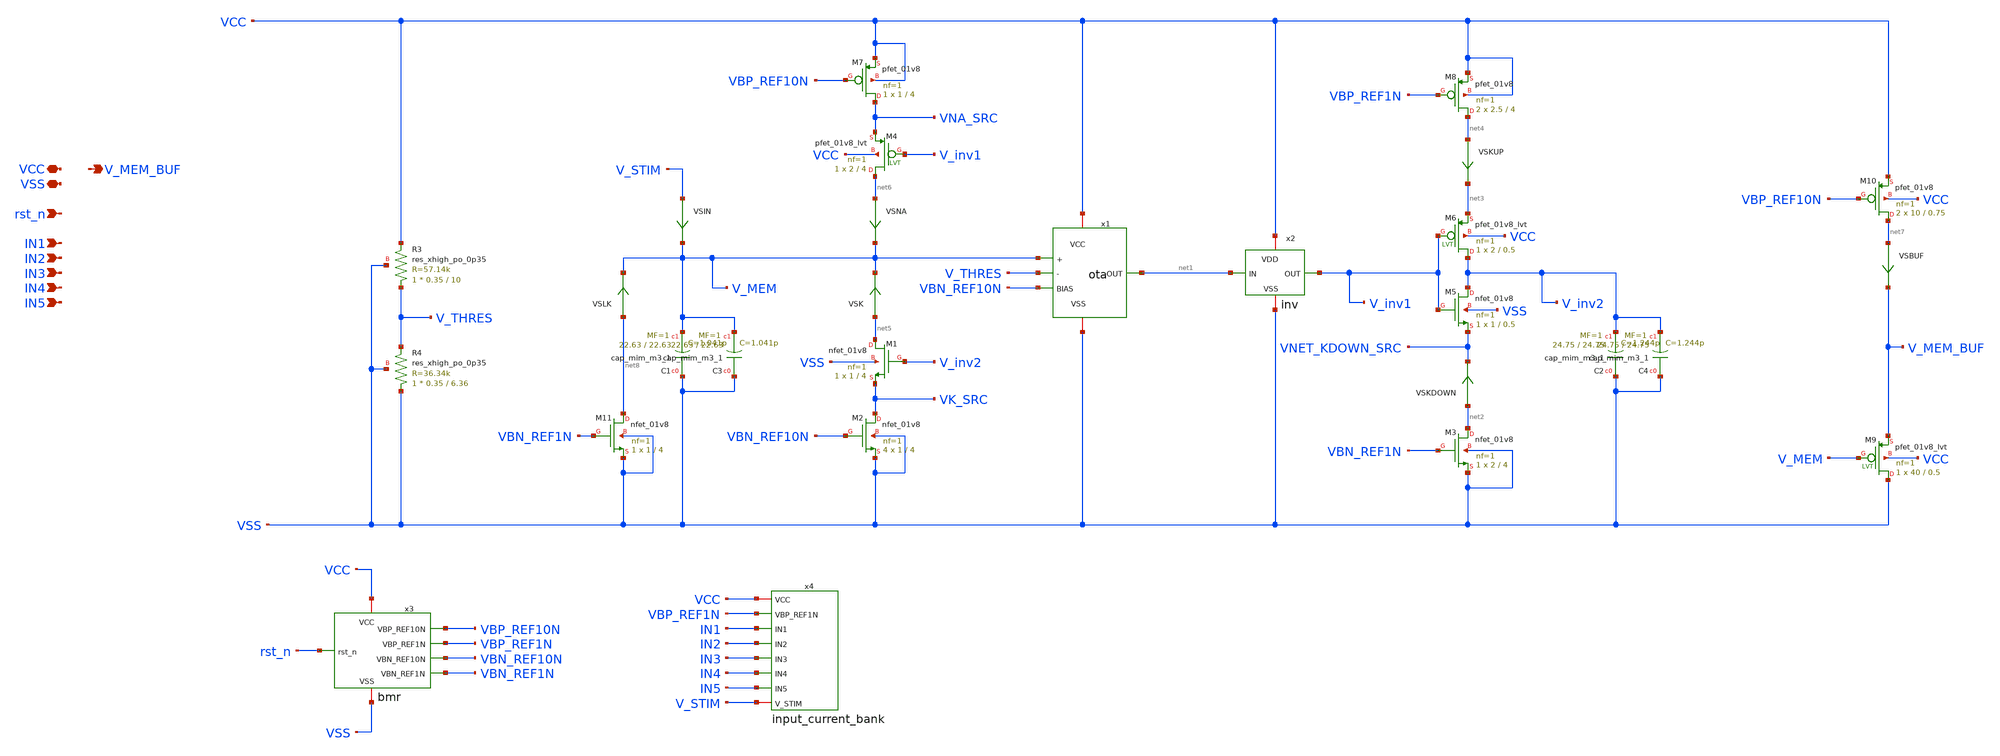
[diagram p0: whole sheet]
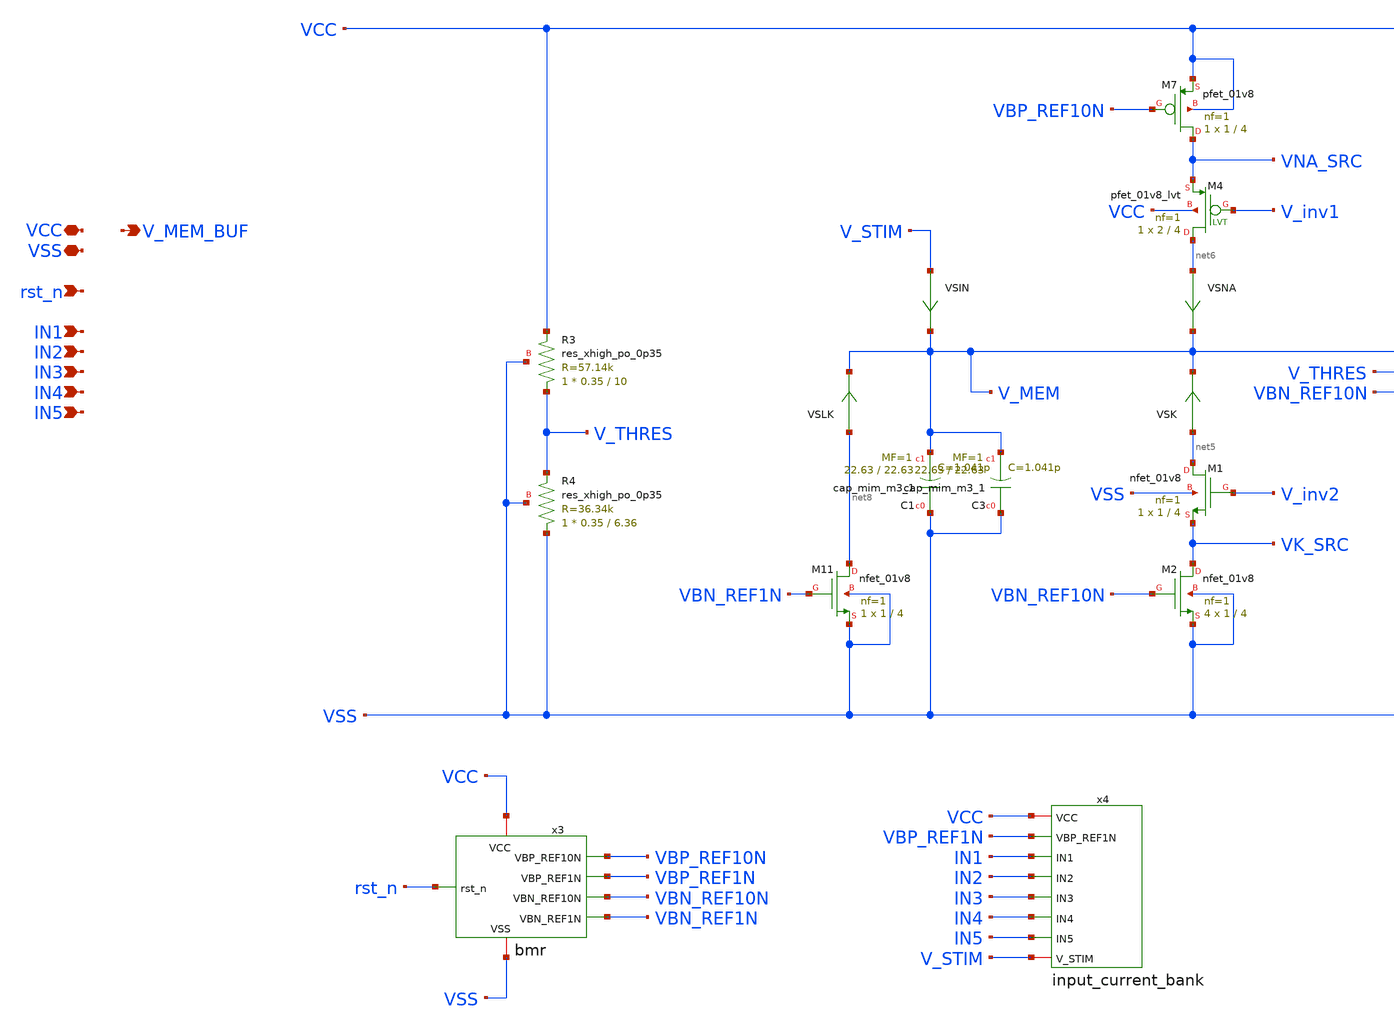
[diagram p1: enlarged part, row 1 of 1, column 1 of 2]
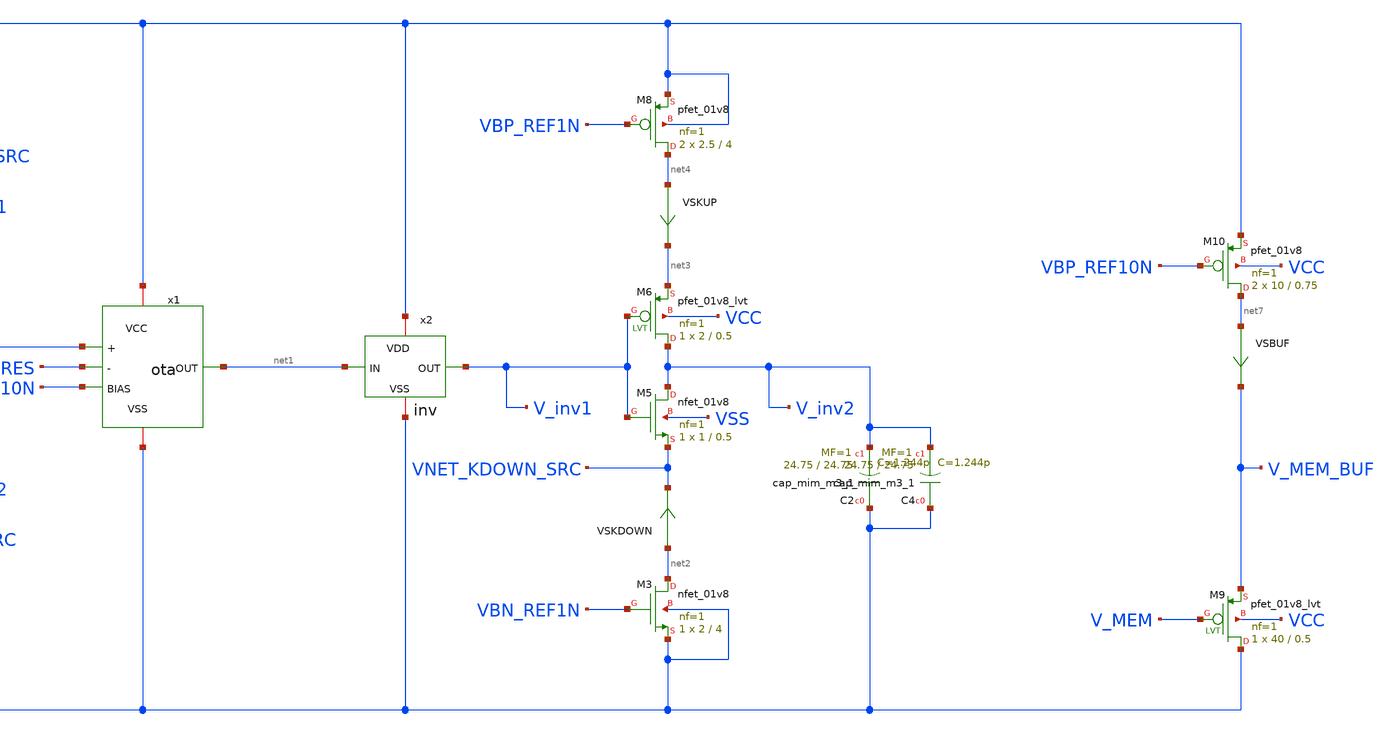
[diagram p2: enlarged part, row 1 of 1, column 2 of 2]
** sch_path: schem/vamp_if_neuron.sch
**.subckt vamp_if_neuron VCC VSS rst_n V_MEM_BUF IN1 IN2 IN3 IN4 IN5
*.iopin VCC
*.iopin VSS
*.ipin rst_n
*.opin V_MEM_BUF
*.ipin IN1
*.ipin IN2
*.ipin IN3
*.ipin IN4
*.ipin IN5
x1 VCC net1 VSS VBN_REF10N V_MEM V_THRES ota
x2 VCC net1 V_inv1 VSS inv
XC1 VSS V_MEM sky130_fd_pr__cap_mim_m3_1 W=22.63 L=22.63 MF=1 m=1
XM1 net5 V_inv2 VK_SRC VSS sky130_fd_pr__nfet_01v8 L=4 W=1 nf=1 ad='int((1 + 1)/2) * 1 / 1 * 0.29' as='int((1 + 2)/2) * 1 / 1 * 0.29'
+ pd='2*int((1 + 1)/2) * (1 / 1 + 0.29)' ps='2*int((1 + 2)/2) * (1 / 1 + 0.29)' nrd='0.29 / 1 ' nrs='0.29 / 1 '
+ sa=0 sb=0 sd=0 mult=1 m=1
XM5 V_inv2 V_inv1 VNET_KDOWN_SRC VSS sky130_fd_pr__nfet_01v8 L=0.5 W=1 nf=1 ad='int((1 + 1)/2) * 1 / 1 * 0.29'
+ as='int((1 + 2)/2) * 1 / 1 * 0.29' pd='2*int((1 + 1)/2) * (1 / 1 + 0.29)' ps='2*int((1 + 2)/2) * (1 / 1 + 0.29)'
+ nrd='0.29 / 1 ' nrs='0.29 / 1 ' sa=0 sb=0 sd=0 mult=1 m=1
XM6 V_inv2 V_inv1 net3 VCC sky130_fd_pr__pfet_01v8_lvt L=0.5 W=2 nf=1 ad='int((1 + 1)/2) * 2 / 1 * 0.29'
+ as='int((1 + 2)/2) * 2 / 1 * 0.29' pd='2*int((1 + 1)/2) * (2 / 1 + 0.29)' ps='2*int((1 + 2)/2) * (2 / 1 + 0.29)'
+ nrd='0.29 / 2 ' nrs='0.29 / 2 ' sa=0 sb=0 sd=0 mult=1 m=1
XC2 VSS V_inv2 sky130_fd_pr__cap_mim_m3_1 W=24.75 L=24.75 MF=1 m=1
VSNA net6 V_MEM 0
.save i(vsna)
VSKUP net4 net3 0
.save i(vskup)
VSK net5 V_MEM 0
.save i(vsk)
VSKDOWN net2 VNET_KDOWN_SRC 0
.save i(vskdown)
XM2 VK_SRC VBN_REF10N VSS VSS sky130_fd_pr__nfet_01v8 L=4 W=1 nf=1 ad='int((1 + 1)/2) * 1 / 1 * 0.29'
+ as='int((1 + 2)/2) * 1 / 1 * 0.29' pd='2*int((1 + 1)/2) * (1 / 1 + 0.29)' ps='2*int((1 + 2)/2) * (1 / 1 + 0.29)'
+ nrd='0.29 / 1 ' nrs='0.29 / 1 ' sa=0 sb=0 sd=0 mult=4 m=4
XM3 net2 VBN_REF1N VSS VSS sky130_fd_pr__nfet_01v8 L=4 W=2 nf=1 ad='int((1 + 1)/2) * 2 / 1 * 0.29' as='int((1 + 2)/2) * 2 / 1 * 0.29'
+ pd='2*int((1 + 1)/2) * (2 / 1 + 0.29)' ps='2*int((1 + 2)/2) * (2 / 1 + 0.29)' nrd='0.29 / 2 ' nrs='0.29 / 2 '
+ sa=0 sb=0 sd=0 mult=1 m=1
XM7 VNA_SRC VBP_REF10N VCC VCC sky130_fd_pr__pfet_01v8 L=4 W=1 nf=1 ad='int((1 + 1)/2) * 1 / 1 * 0.29'
+ as='int((1 + 2)/2) * 1 / 1 * 0.29' pd='2*int((1 + 1)/2) * (1 / 1 + 0.29)' ps='2*int((1 + 2)/2) * (1 / 1 + 0.29)'
+ nrd='0.29 / 1 ' nrs='0.29 / 1 ' sa=0 sb=0 sd=0 mult=1 m=1
XM8 net4 VBP_REF1N VCC VCC sky130_fd_pr__pfet_01v8 L=4 W=2.5 nf=1 ad='int((1 + 1)/2) * 2.5 / 1 * 0.29'
+ as='int((1 + 2)/2) * 2.5 / 1 * 0.29' pd='2*int((1 + 1)/2) * (2.5 / 1 + 0.29)' ps='2*int((1 + 2)/2) * (2.5 / 1 + 0.29)'
+ nrd='0.29 / 2.5 ' nrs='0.29 / 2.5 ' sa=0 sb=0 sd=0 mult=2 m=2
XM4 net6 V_inv1 VNA_SRC VCC sky130_fd_pr__pfet_01v8_lvt L=4 W=2 nf=1 ad='int((1 + 1)/2) * 2 / 1 * 0.29'
+ as='int((1 + 2)/2) * 2 / 1 * 0.29' pd='2*int((1 + 1)/2) * (2 / 1 + 0.29)' ps='2*int((1 + 2)/2) * (2 / 1 + 0.29)'
+ nrd='0.29 / 2 ' nrs='0.29 / 2 ' sa=0 sb=0 sd=0 mult=1 m=1
VSIN V_STIM V_MEM 0
.save i(vsin)
x3 VCC VBP_REF10N VSS VBP_REF1N VBN_REF10N VBN_REF1N rst_n bmr
VSBUF net7 V_MEM_BUF 0
.save i(vsbuf)
XM9 VSS V_MEM V_MEM_BUF VCC sky130_fd_pr__pfet_01v8_lvt L=0.5 W=40 nf=1 ad='int((1 + 1)/2) * 40 / 1 * 0.29'
+ as='int((1 + 2)/2) * 40 / 1 * 0.29' pd='2*int((1 + 1)/2) * (40 / 1 + 0.29)' ps='2*int((1 + 2)/2) * (40 / 1 + 0.29)'
+ nrd='0.29 / 40 ' nrs='0.29 / 40 ' sa=0 sb=0 sd=0 mult=1 m=1
XM10 net7 VBP_REF10N VCC VCC sky130_fd_pr__pfet_01v8 L=0.75 W=10 nf=1 ad='int((1 + 1)/2) * 10 / 1 * 0.29'
+ as='int((1 + 2)/2) * 10 / 1 * 0.29' pd='2*int((1 + 1)/2) * (10 / 1 + 0.29)' ps='2*int((1 + 2)/2) * (10 / 1 + 0.29)'
+ nrd='0.29 / 10 ' nrs='0.29 / 10 ' sa=0 sb=0 sd=0 mult=2 m=2
XM11 net8 VBN_REF1N VSS VSS sky130_fd_pr__nfet_01v8 L=4 W=1 nf=1 ad='int((1 + 1)/2) * 1 / 1 * 0.29' as='int((1 + 2)/2) * 1 / 1 * 0.29'
+ pd='2*int((1 + 1)/2) * (1 / 1 + 0.29)' ps='2*int((1 + 2)/2) * (1 / 1 + 0.29)' nrd='0.29 / 1 ' nrs='0.29 / 1 '
+ sa=0 sb=0 sd=0 mult=1 m=1
VSLK net8 V_MEM 0
.save i(vslk)
XR3 V_THRES VCC VSS sky130_fd_pr__res_xhigh_po_0p35 L=10 mult=1 m=1
XR4 VSS V_THRES VSS sky130_fd_pr__res_xhigh_po_0p35 L=6.36 mult=1 m=1
x4 VCC V_STIM VBP_REF1N IN1 IN2 IN3 IN4 IN5 input_current_bank
XC3 VSS V_MEM sky130_fd_pr__cap_mim_m3_1 W=22.63 L=22.63 MF=1 m=1
XC4 VSS V_inv2 sky130_fd_pr__cap_mim_m3_1 W=24.75 L=24.75 MF=1 m=1
**.ends

* expanding   symbol:  ota/ota.sym # of pins=6
** sym_path: schem/ota/ota.sym
** sch_path: schem/ota/ota.sch
.subckt ota VCC OUT VSS BIAS + -
*.ipin BIAS
*.ipin +
*.ipin -
*.opin OUT
*.iopin VCC
*.iopin VSS
XM1 VSRC + VBOT VSS sky130_fd_pr__nfet_01v8 L=0.5 W=1 nf=1 ad='int((1 + 1)/2) * 1 / 1 * 0.29' as='int((1 + 2)/2) * 1 / 1 * 0.29'
+ pd='2*int((1 + 1)/2) * (1 / 1 + 0.29)' ps='2*int((1 + 2)/2) * (1 / 1 + 0.29)' nrd='0.29 / 1 ' nrs='0.29 / 1 '
+ sa=0 sb=0 sd=0 mult=1 m=1
XM2 OUT - VBOT VSS sky130_fd_pr__nfet_01v8 L=0.5 W=1 nf=1 ad='int((1 + 1)/2) * 1 / 1 * 0.29' as='int((1 + 2)/2) * 1 / 1 * 0.29'
+ pd='2*int((1 + 1)/2) * (1 / 1 + 0.29)' ps='2*int((1 + 2)/2) * (1 / 1 + 0.29)' nrd='0.29 / 1 ' nrs='0.29 / 1 '
+ sa=0 sb=0 sd=0 mult=1 m=1
XM3 VSRC VSRC VCC VCC sky130_fd_pr__pfet_01v8_lvt L=0.5 W=2 nf=1 ad='int((1 + 1)/2) * 2 / 1 * 0.29' as='int((1 + 2)/2) * 2 / 1 * 0.29'
+ pd='2*int((1 + 1)/2) * (2 / 1 + 0.29)' ps='2*int((1 + 2)/2) * (2 / 1 + 0.29)' nrd='0.29 / 2 ' nrs='0.29 / 2 '
+ sa=0 sb=0 sd=0 mult=1 m=1
XM4 OUT VSRC VCC VCC sky130_fd_pr__pfet_01v8_lvt L=0.5 W=2 nf=1 ad='int((1 + 1)/2) * 2 / 1 * 0.29' as='int((1 + 2)/2) * 2 / 1 * 0.29'
+ pd='2*int((1 + 1)/2) * (2 / 1 + 0.29)' ps='2*int((1 + 2)/2) * (2 / 1 + 0.29)' nrd='0.29 / 2 ' nrs='0.29 / 2 '
+ sa=0 sb=0 sd=0 mult=1 m=1
XM5 VBOT BIAS VSS VSS sky130_fd_pr__nfet_01v8 L=0.5 W=1 nf=1 ad='int((1 + 1)/2) * 1 / 1 * 0.29' as='int((1 + 2)/2) * 1 / 1 * 0.29'
+ pd='2*int((1 + 1)/2) * (1 / 1 + 0.29)' ps='2*int((1 + 2)/2) * (1 / 1 + 0.29)' nrd='0.29 / 1 ' nrs='0.29 / 1 '
+ sa=0 sb=0 sd=0 mult=1 m=1
.ends


* expanding   symbol:  inv/inv.sym # of pins=4
** sym_path: schem/inv/inv.sym
** sch_path: schem/inv/inv.sch
.subckt inv VDD IN OUT VSS
*.ipin IN
*.iopin VDD
*.iopin VSS
*.opin OUT
XM1 OUT IN VSS VSS sky130_fd_pr__nfet_01v8 L=0.5 W=1 nf=1 ad='int((1 + 1)/2) * 1 / 1 * 0.29' as='int((1 + 2)/2) * 1 / 1 * 0.29'
+ pd='2*int((1 + 1)/2) * (1 / 1 + 0.29)' ps='2*int((1 + 2)/2) * (1 / 1 + 0.29)' nrd='0.29 / 1 ' nrs='0.29 / 1 '
+ sa=0 sb=0 sd=0 mult=1 m=1
XM2 OUT IN VDD VDD sky130_fd_pr__pfet_01v8_lvt L=0.5 W=2 nf=1 ad='int((1 + 1)/2) * 2 / 1 * 0.29' as='int((1 + 2)/2) * 2 / 1 * 0.29'
+ pd='2*int((1 + 1)/2) * (2 / 1 + 0.29)' ps='2*int((1 + 2)/2) * (2 / 1 + 0.29)' nrd='0.29 / 2 ' nrs='0.29 / 2 '
+ sa=0 sb=0 sd=0 mult=1 m=1
.ends


* expanding   symbol:  bias/bmr.sym # of pins=7
** sym_path: schem/bias/bmr.sym
** sch_path: schem/bias/bmr.sch
.subckt bmr VCC VBP_REF10N VSS VBP_REF1N VBN_REF10N VBN_REF1N rst_n
*.iopin VCC
*.iopin VSS
*.ipin rst_n
*.opin VBP_REF10N
*.opin VBP_REF1N
*.opin VBN_REF10N
*.opin VBN_REF1N
x1 VCC VBP_REF10N VSS VBN_REF10N rst_n bmr_10n
XM1 net1 VBP_REF10N VCC VCC sky130_fd_pr__pfet_01v8 L=4 W=1 nf=1 ad='int((1 + 1)/2) * 1 / 1 * 0.29' as='int((1 + 2)/2) * 1 / 1 * 0.29'
+ pd='2*int((1 + 1)/2) * (1 / 1 + 0.29)' ps='2*int((1 + 2)/2) * (1 / 1 + 0.29)' nrd='0.29 / 1 ' nrs='0.29 / 1 '
+ sa=0 sb=0 sd=0 mult=1 m=1
XM2 VBN_REF1N VBN_REF1N VSS VSS sky130_fd_pr__nfet_01v8 L=4 W=1 nf=1 ad='int((1 + 1)/2) * 1 / 1 * 0.29'
+ as='int((1 + 2)/2) * 1 / 1 * 0.29' pd='2*int((1 + 1)/2) * (1 / 1 + 0.29)' ps='2*int((1 + 2)/2) * (1 / 1 + 0.29)'
+ nrd='0.29 / 1 ' nrs='0.29 / 1 ' sa=0 sb=0 sd=0 mult=10 m=10
XM3 net2 VBN_REF1N VSS VSS sky130_fd_pr__nfet_01v8 L=4 W=1 nf=1 ad='int((1 + 1)/2) * 1 / 1 * 0.29' as='int((1 + 2)/2) * 1 / 1 * 0.29'
+ pd='2*int((1 + 1)/2) * (1 / 1 + 0.29)' ps='2*int((1 + 2)/2) * (1 / 1 + 0.29)' nrd='0.29 / 1 ' nrs='0.29 / 1 '
+ sa=0 sb=0 sd=0 mult=1 m=1
XM4 VBP_REF1N VBP_REF1N VCC VCC sky130_fd_pr__pfet_01v8 L=4 W=1 nf=1 ad='int((1 + 1)/2) * 1 / 1 * 0.29'
+ as='int((1 + 2)/2) * 1 / 1 * 0.29' pd='2*int((1 + 1)/2) * (1 / 1 + 0.29)' ps='2*int((1 + 2)/2) * (1 / 1 + 0.29)'
+ nrd='0.29 / 1 ' nrs='0.29 / 1 ' sa=0 sb=0 sd=0 mult=1 m=1
Vmeas net1 VBN_REF1N 0
.save i(vmeas)
Vmeas1 VBP_REF1N net2 0
.save i(vmeas1)
.ends


* expanding   symbol:  input_current_bank.sym # of pins=8
** sym_path: schem/input_current_bank.sym
** sch_path: schem/input_current_bank.sch
.subckt input_current_bank VCC V_STIM VBP_REF1N IN1 IN2 IN3 IN4 IN5
*.iopin VCC
*.iopin V_STIM
*.ipin VBP_REF1N
*.ipin IN1
*.ipin IN2
*.ipin IN3
*.ipin IN4
*.ipin IN5
X0.5 net1 VBP_REF1N VCC VCC sky130_fd_pr__pfet_01v8 L=16 W=0.5 nf=1 ad='int((1 + 1)/2) * 0.5 / 1 * 0.29'
+ as='int((1 + 2)/2) * 0.5 / 1 * 0.29' pd='2*int((1 + 1)/2) * (0.5 / 1 + 0.29)' ps='2*int((1 + 2)/2) * (0.5 / 1 + 0.29)'
+ nrd='0.29 / 0.5 ' nrs='0.29 / 0.5 ' sa=0 sb=0 sd=0 mult=1 m=1
XM13 V_STIM IN1 net1 VCC sky130_fd_pr__pfet_01v8_lvt L=4 W=2 nf=1 ad='int((1 + 1)/2) * 2 / 1 * 0.29'
+ as='int((1 + 2)/2) * 2 / 1 * 0.29' pd='2*int((1 + 1)/2) * (2 / 1 + 0.29)' ps='2*int((1 + 2)/2) * (2 / 1 + 0.29)'
+ nrd='0.29 / 2 ' nrs='0.29 / 2 ' sa=0 sb=0 sd=0 mult=1 m=1
XM14 net2 VBP_REF1N VCC VCC sky130_fd_pr__pfet_01v8 L=8 W=0.5 nf=1 ad='int((1 + 1)/2) * 0.5 / 1 * 0.29'
+ as='int((1 + 2)/2) * 0.5 / 1 * 0.29' pd='2*int((1 + 1)/2) * (0.5 / 1 + 0.29)' ps='2*int((1 + 2)/2) * (0.5 / 1 + 0.29)'
+ nrd='0.29 / 0.5 ' nrs='0.29 / 0.5 ' sa=0 sb=0 sd=0 mult=1 m=1
XM15 V_STIM IN2 net2 VCC sky130_fd_pr__pfet_01v8_lvt L=4 W=2 nf=1 ad='int((1 + 1)/2) * 2 / 1 * 0.29'
+ as='int((1 + 2)/2) * 2 / 1 * 0.29' pd='2*int((1 + 1)/2) * (2 / 1 + 0.29)' ps='2*int((1 + 2)/2) * (2 / 1 + 0.29)'
+ nrd='0.29 / 2 ' nrs='0.29 / 2 ' sa=0 sb=0 sd=0 mult=1 m=1
XM16 net3 VBP_REF1N VCC VCC sky130_fd_pr__pfet_01v8 L=4 W=1 nf=1 ad='int((1 + 1)/2) * 1 / 1 * 0.29' as='int((1 + 2)/2) * 1 / 1 * 0.29'
+ pd='2*int((1 + 1)/2) * (1 / 1 + 0.29)' ps='2*int((1 + 2)/2) * (1 / 1 + 0.29)' nrd='0.29 / 1 ' nrs='0.29 / 1 '
+ sa=0 sb=0 sd=0 mult=1 m=1
XM17 V_STIM IN3 net3 VCC sky130_fd_pr__pfet_01v8_lvt L=4 W=2 nf=1 ad='int((1 + 1)/2) * 2 / 1 * 0.29'
+ as='int((1 + 2)/2) * 2 / 1 * 0.29' pd='2*int((1 + 1)/2) * (2 / 1 + 0.29)' ps='2*int((1 + 2)/2) * (2 / 1 + 0.29)'
+ nrd='0.29 / 2 ' nrs='0.29 / 2 ' sa=0 sb=0 sd=0 mult=1 m=1
XM18 net4 VBP_REF1N VCC VCC sky130_fd_pr__pfet_01v8 L=4 W=1 nf=1 ad='int((1 + 1)/2) * 1 / 1 * 0.29' as='int((1 + 2)/2) * 1 / 1 * 0.29'
+ pd='2*int((1 + 1)/2) * (1 / 1 + 0.29)' ps='2*int((1 + 2)/2) * (1 / 1 + 0.29)' nrd='0.29 / 1 ' nrs='0.29 / 1 '
+ sa=0 sb=0 sd=0 mult=1 m=1
XM19 V_STIM IN4 net4 VCC sky130_fd_pr__pfet_01v8_lvt L=4 W=2 nf=1 ad='int((1 + 1)/2) * 2 / 1 * 0.29'
+ as='int((1 + 2)/2) * 2 / 1 * 0.29' pd='2*int((1 + 1)/2) * (2 / 1 + 0.29)' ps='2*int((1 + 2)/2) * (2 / 1 + 0.29)'
+ nrd='0.29 / 2 ' nrs='0.29 / 2 ' sa=0 sb=0 sd=0 mult=1 m=1
XM20 net5 VBP_REF1N VCC VCC sky130_fd_pr__pfet_01v8 L=4 W=1 nf=1 ad='int((1 + 1)/2) * 1 / 1 * 0.29' as='int((1 + 2)/2) * 1 / 1 * 0.29'
+ pd='2*int((1 + 1)/2) * (1 / 1 + 0.29)' ps='2*int((1 + 2)/2) * (1 / 1 + 0.29)' nrd='0.29 / 1 ' nrs='0.29 / 1 '
+ sa=0 sb=0 sd=0 mult=2 m=2
XM21 V_STIM IN5 net5 VCC sky130_fd_pr__pfet_01v8_lvt L=4 W=2 nf=1 ad='int((1 + 1)/2) * 2 / 1 * 0.29'
+ as='int((1 + 2)/2) * 2 / 1 * 0.29' pd='2*int((1 + 1)/2) * (2 / 1 + 0.29)' ps='2*int((1 + 2)/2) * (2 / 1 + 0.29)'
+ nrd='0.29 / 2 ' nrs='0.29 / 2 ' sa=0 sb=0 sd=0 mult=1 m=1
.ends


* expanding   symbol:  bias/bmr_10n.sym # of pins=5
** sym_path: schem/bias/bmr_10n.sym
** sch_path: schem/bias/bmr_10n.sch
.subckt bmr_10n VCC VBP VSS VBN rst_n
*.iopin VCC
*.iopin VSS
*.ipin rst_n
*.opin VBP
*.opin VBN
XM1 VBP VBP VCC VCC sky130_fd_pr__pfet_01v8 L=4 W=1 nf=1 ad='int((1 + 1)/2) * 1 / 1 * 0.29' as='int((1 + 2)/2) * 1 / 1 * 0.29'
+ pd='2*int((1 + 1)/2) * (1 / 1 + 0.29)' ps='2*int((1 + 2)/2) * (1 / 1 + 0.29)' nrd='0.29 / 1 ' nrs='0.29 / 1 '
+ sa=0 sb=0 sd=0 mult=1 m=1
XM2 net3 VBP VCC VCC sky130_fd_pr__pfet_01v8 L=4 W=1 nf=1 ad='int((1 + 1)/2) * 1 / 1 * 0.29' as='int((1 + 2)/2) * 1 / 1 * 0.29'
+ pd='2*int((1 + 1)/2) * (1 / 1 + 0.29)' ps='2*int((1 + 2)/2) * (1 / 1 + 0.29)' nrd='0.29 / 1 ' nrs='0.29 / 1 '
+ sa=0 sb=0 sd=0 mult=1 m=1
XM3 net2 VBN net1 VSS sky130_fd_pr__nfet_01v8 L=4 W=8 nf=1 ad='int((1 + 1)/2) * 8 / 1 * 0.29' as='int((1 + 2)/2) * 8 / 1 * 0.29'
+ pd='2*int((1 + 1)/2) * (8 / 1 + 0.29)' ps='2*int((1 + 2)/2) * (8 / 1 + 0.29)' nrd='0.29 / 8 ' nrs='0.29 / 8 '
+ sa=0 sb=0 sd=0 mult=1 m=1
XM4 VBN VBN VSS VSS sky130_fd_pr__nfet_01v8 L=4 W=1 nf=1 ad='int((1 + 1)/2) * 1 / 1 * 0.29' as='int((1 + 2)/2) * 1 / 1 * 0.29'
+ pd='2*int((1 + 1)/2) * (1 / 1 + 0.29)' ps='2*int((1 + 2)/2) * (1 / 1 + 0.29)' nrd='0.29 / 1 ' nrs='0.29 / 1 '
+ sa=0 sb=0 sd=0 mult=1 m=1
XR1 net5 net1 net4 sky130_fd_pr__res_xhigh_po_0p35 L={LR} mult=1 m=1
VSRIGHT VBP net2 0
.save i(vsright)
VSLEFT net3 VBN 0
.save i(vsleft)
XM5 VBN rst_n VCC VCC sky130_fd_pr__pfet_01v8 L=4 W=1 nf=1 ad='int((1 + 1)/2) * 1 / 1 * 0.29' as='int((1 + 2)/2) * 1 / 1 * 0.29'
+ pd='2*int((1 + 1)/2) * (1 / 1 + 0.29)' ps='2*int((1 + 2)/2) * (1 / 1 + 0.29)' nrd='0.29 / 1 ' nrs='0.29 / 1 '
+ sa=0 sb=0 sd=0 mult=1 m=1
XR2 net6 net5 net4 sky130_fd_pr__res_xhigh_po_0p35 L={LR} mult=1 m=1
XR3 net7 net6 net4 sky130_fd_pr__res_xhigh_po_0p35 L={LR} mult=1 m=1
XR4 net8 net7 net4 sky130_fd_pr__res_xhigh_po_0p35 L={LR} mult=1 m=1
XR5 net9 net8 net4 sky130_fd_pr__res_xhigh_po_0p35 L={LR} mult=1 m=1
XR6 net10 net9 net4 sky130_fd_pr__res_xhigh_po_0p35 L={LR} mult=1 m=1
XR7 net11 net10 net4 sky130_fd_pr__res_xhigh_po_0p35 L={LR} mult=1 m=1
XR8 VSS net11 net4 sky130_fd_pr__res_xhigh_po_0p35 L={LR} mult=1 m=1
**** begin user architecture code


.param LR=1084/8


**** end user architecture code
.ends

.end
